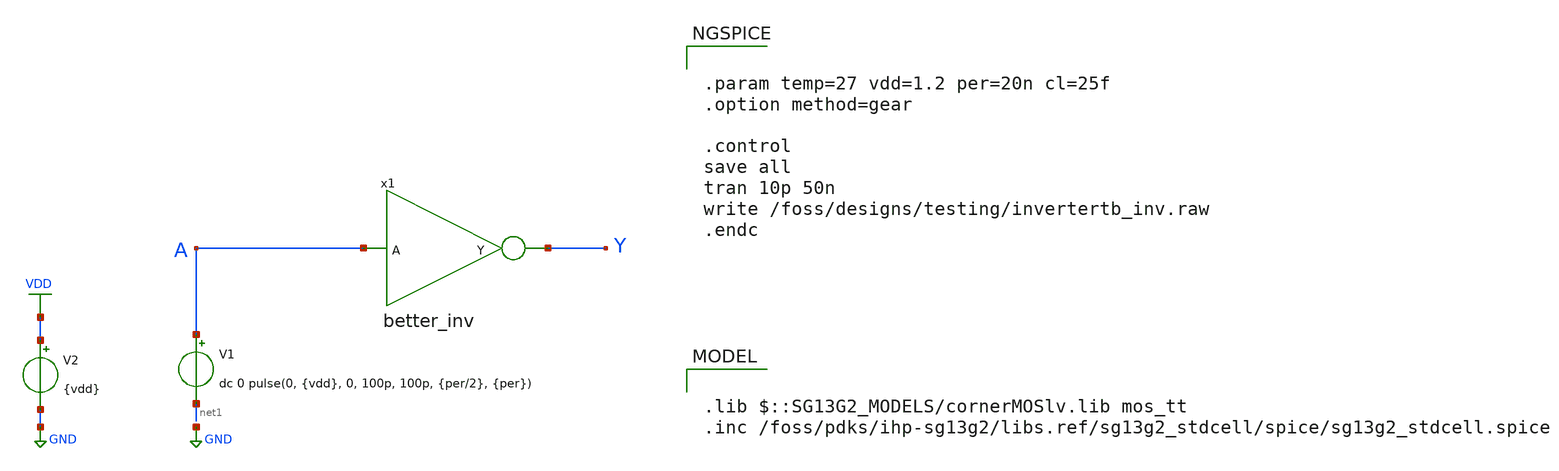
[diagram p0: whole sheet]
** sch_path: zip_meiners/ic_design/design_clkgen/inverter/tb_inverter.sch
**.subckt tb_inverter
x1 Y A better_inv
V1 A net1 dc 0 pulse(0, {vdd}, 0, 100p, 100p, {per/2}, {per})
V2 VDD GND {vdd}
**** begin user architecture code

.lib $::SG13G2_MODELS/cornerMOSlv.lib mos_tt
.inc /foss/pdks/ihp-sg13g2/libs.ref/sg13g2_stdcell/spice/sg13g2_stdcell.spice



.param temp=27 vdd=1.2 per=20n cl=25f
.option method=gear

.control
save all
tran 10p 50n
write /foss/designs/testing/invertertb_inv.raw
.endc


**** end user architecture code
**.ends
.GLOBAL GND
.GLOBAL VDD
.end
